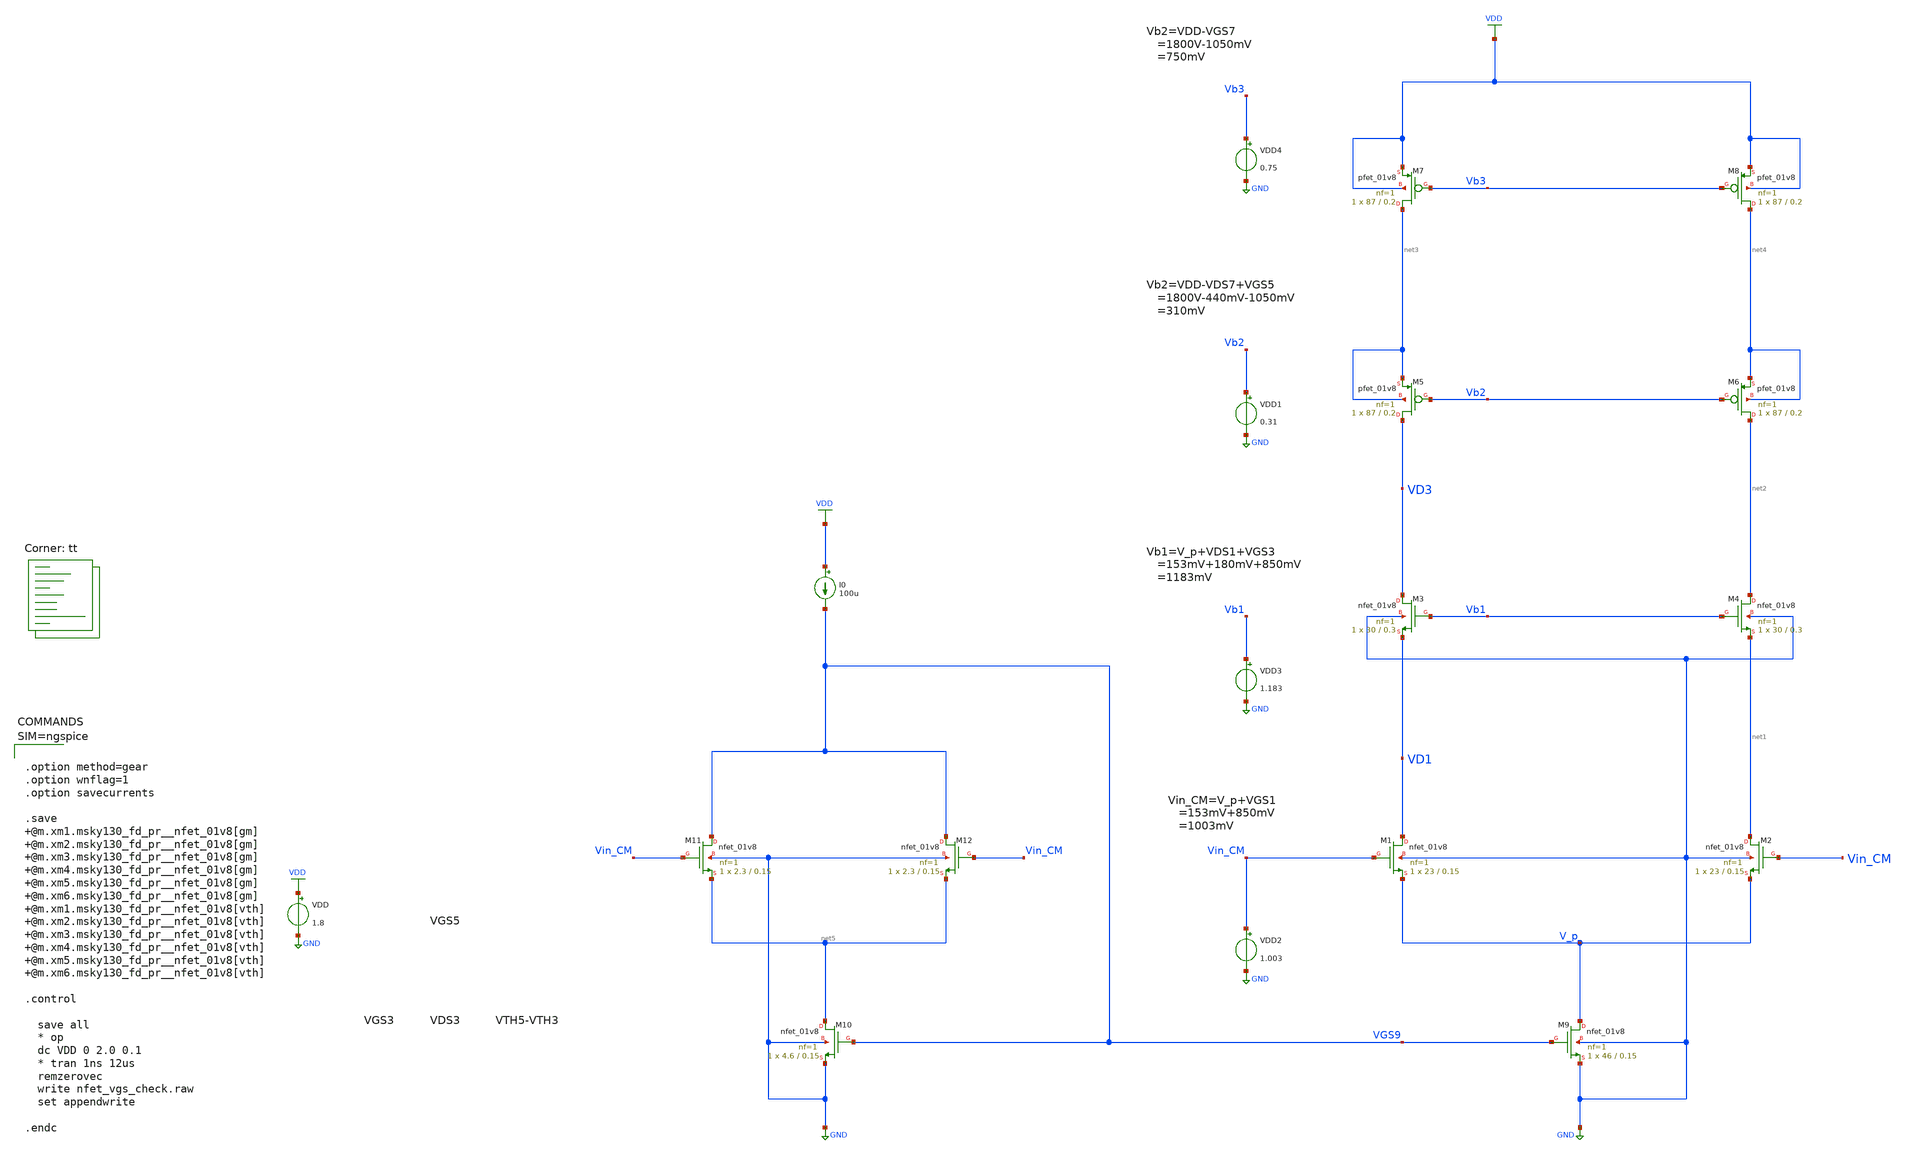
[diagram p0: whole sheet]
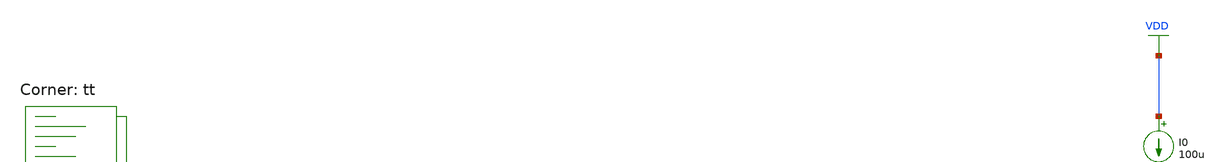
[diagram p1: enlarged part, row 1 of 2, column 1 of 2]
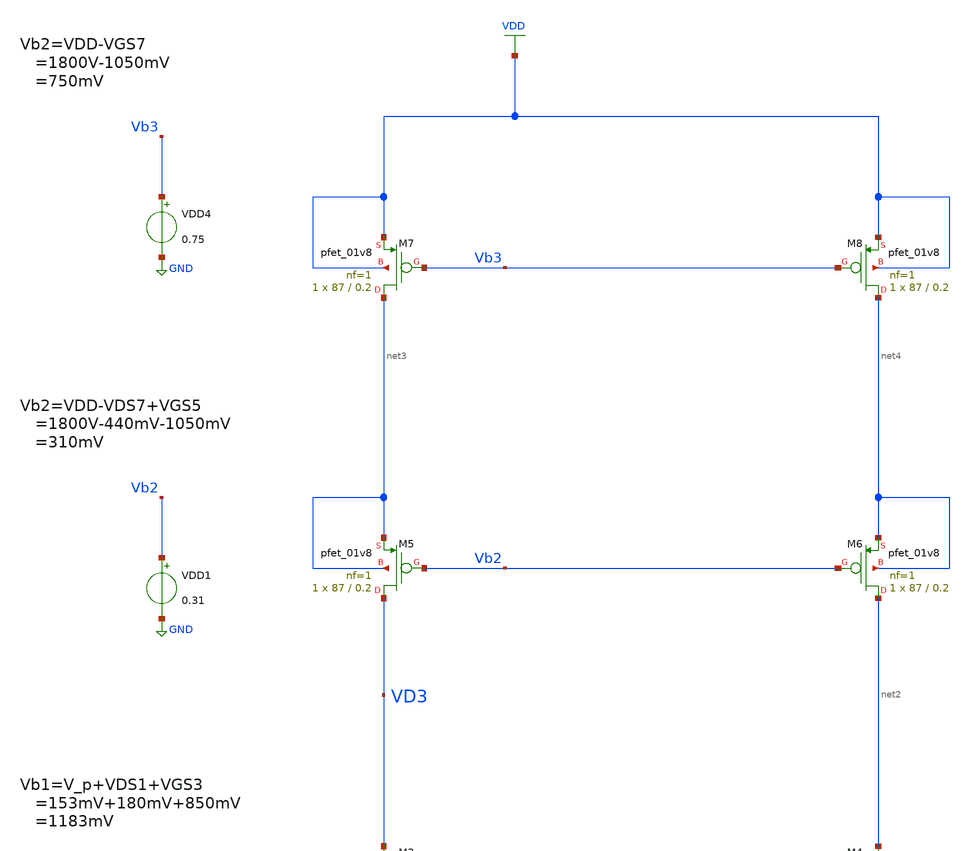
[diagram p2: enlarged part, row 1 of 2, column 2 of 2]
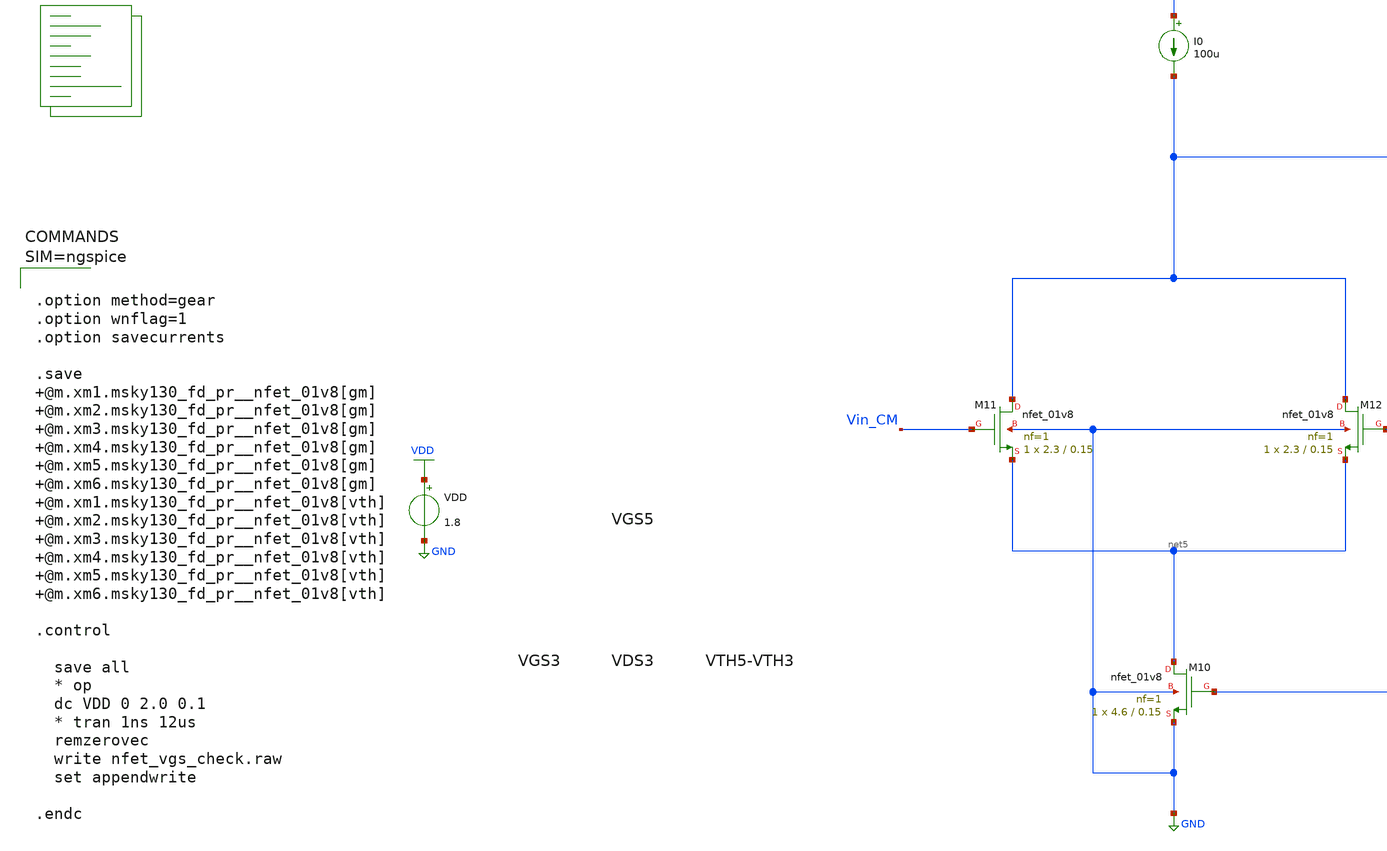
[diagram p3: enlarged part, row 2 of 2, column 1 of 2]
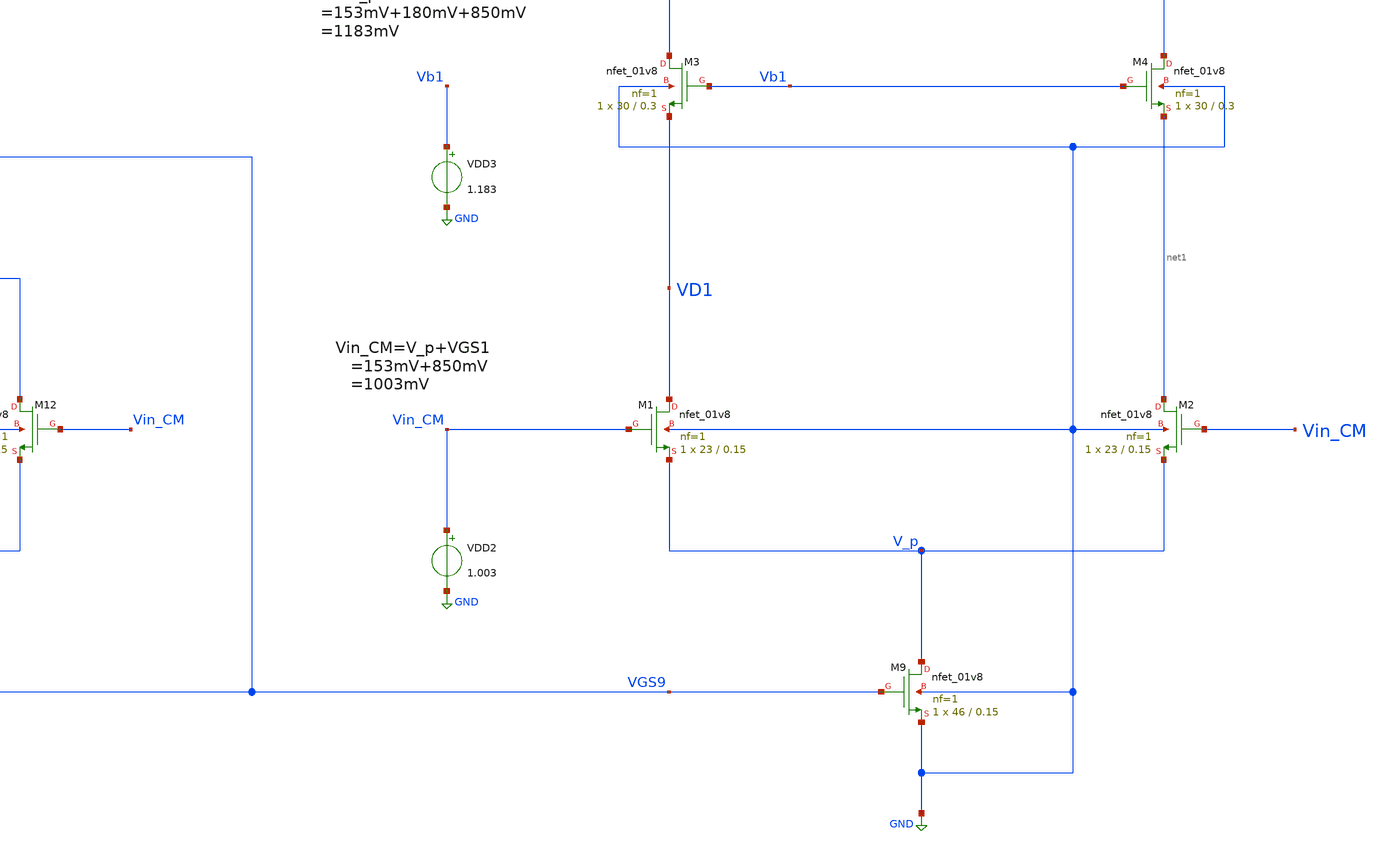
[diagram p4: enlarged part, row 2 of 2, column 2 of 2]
** sch_path: projects/opamp/xschem_ngspice/nfet_vgs_check.sch
**.subckt nfet_vgs_check
VDD VDD GND 1.8
XM1 VD1 Vin_CM V_p GND sky130_fd_pr__nfet_01v8 L=0.15 W=23 nf=1 ad='int((nf+1)/2) * W/nf * 0.29' as='int((nf+2)/2) * W/nf * 0.29'
+ pd='2*int((nf+1)/2) * (W/nf + 0.29)' ps='2*int((nf+2)/2) * (W/nf + 0.29)' nrd='0.29 / W' nrs='0.29 / W'
+ sa=0 sb=0 sd=0 mult=1 m=1
XM2 net1 Vin_CM V_p GND sky130_fd_pr__nfet_01v8 L=0.15 W=23 nf=1 ad='int((nf+1)/2) * W/nf * 0.29' as='int((nf+2)/2) * W/nf * 0.29'
+ pd='2*int((nf+1)/2) * (W/nf + 0.29)' ps='2*int((nf+2)/2) * (W/nf + 0.29)' nrd='0.29 / W' nrs='0.29 / W'
+ sa=0 sb=0 sd=0 mult=1 m=1
XM3 VD3 Vb1 VD1 GND sky130_fd_pr__nfet_01v8 L=0.3 W=30 nf=1 ad='int((nf+1)/2) * W/nf * 0.29' as='int((nf+2)/2) * W/nf * 0.29'
+ pd='2*int((nf+1)/2) * (W/nf + 0.29)' ps='2*int((nf+2)/2) * (W/nf + 0.29)' nrd='0.29 / W' nrs='0.29 / W'
+ sa=0 sb=0 sd=0 mult=1 m=1
XM4 net2 Vb1 net1 GND sky130_fd_pr__nfet_01v8 L=0.3 W=30 nf=1 ad='int((nf+1)/2) * W/nf * 0.29' as='int((nf+2)/2) * W/nf * 0.29'
+ pd='2*int((nf+1)/2) * (W/nf + 0.29)' ps='2*int((nf+2)/2) * (W/nf + 0.29)' nrd='0.29 / W' nrs='0.29 / W'
+ sa=0 sb=0 sd=0 mult=1 m=1
XM5 VD3 Vb2 net3 net3 sky130_fd_pr__pfet_01v8 L=0.2 W=87 nf=1 ad='int((nf+1)/2) * W/nf * 0.29' as='int((nf+2)/2) * W/nf * 0.29'
+ pd='2*int((nf+1)/2) * (W/nf + 0.29)' ps='2*int((nf+2)/2) * (W/nf + 0.29)' nrd='0.29 / W' nrs='0.29 / W'
+ sa=0 sb=0 sd=0 mult=1 m=1
XM6 net2 Vb2 net4 net4 sky130_fd_pr__pfet_01v8 L=0.2 W=87 nf=1 ad='int((nf+1)/2) * W/nf * 0.29' as='int((nf+2)/2) * W/nf * 0.29'
+ pd='2*int((nf+1)/2) * (W/nf + 0.29)' ps='2*int((nf+2)/2) * (W/nf + 0.29)' nrd='0.29 / W' nrs='0.29 / W'
+ sa=0 sb=0 sd=0 mult=1 m=1
XM7 net3 Vb3 VDD VDD sky130_fd_pr__pfet_01v8 L=0.2 W=87 nf=1 ad='int((nf+1)/2) * W/nf * 0.29' as='int((nf+2)/2) * W/nf * 0.29'
+ pd='2*int((nf+1)/2) * (W/nf + 0.29)' ps='2*int((nf+2)/2) * (W/nf + 0.29)' nrd='0.29 / W' nrs='0.29 / W'
+ sa=0 sb=0 sd=0 mult=1 m=1
XM8 net4 Vb3 VDD VDD sky130_fd_pr__pfet_01v8 L=0.2 W=87 nf=1 ad='int((nf+1)/2) * W/nf * 0.29' as='int((nf+2)/2) * W/nf * 0.29'
+ pd='2*int((nf+1)/2) * (W/nf + 0.29)' ps='2*int((nf+2)/2) * (W/nf + 0.29)' nrd='0.29 / W' nrs='0.29 / W'
+ sa=0 sb=0 sd=0 mult=1 m=1
XM9 V_p VGS9 GND GND sky130_fd_pr__nfet_01v8 L=0.15 W=46 nf=1 ad='int((nf+1)/2) * W/nf * 0.29' as='int((nf+2)/2) * W/nf * 0.29'
+ pd='2*int((nf+1)/2) * (W/nf + 0.29)' ps='2*int((nf+2)/2) * (W/nf + 0.29)' nrd='0.29 / W' nrs='0.29 / W'
+ sa=0 sb=0 sd=0 mult=1 m=1
VDD2 Vin_CM GND 1.003
VDD3 Vb1 GND 1.183
VDD1 Vb2 GND 0.31
VDD4 Vb3 GND 0.75
XM10 net5 VGS9 GND GND sky130_fd_pr__nfet_01v8 L=0.15 W=4.6 nf=1 ad='int((nf+1)/2) * W/nf * 0.29' as='int((nf+2)/2) * W/nf * 0.29'
+ pd='2*int((nf+1)/2) * (W/nf + 0.29)' ps='2*int((nf+2)/2) * (W/nf + 0.29)' nrd='0.29 / W' nrs='0.29 / W'
+ sa=0 sb=0 sd=0 mult=1 m=1
I0 VDD VGS9 100u
XM11 VGS9 Vin_CM net5 GND sky130_fd_pr__nfet_01v8 L=0.15 W=2.3 nf=1 ad='int((nf+1)/2) * W/nf * 0.29'
+ as='int((nf+2)/2) * W/nf * 0.29' pd='2*int((nf+1)/2) * (W/nf + 0.29)' ps='2*int((nf+2)/2) * (W/nf + 0.29)'
+ nrd='0.29 / W' nrs='0.29 / W' sa=0 sb=0 sd=0 mult=1 m=1
XM12 VGS9 Vin_CM net5 GND sky130_fd_pr__nfet_01v8 L=0.15 W=2.3 nf=1 ad='int((nf+1)/2) * W/nf * 0.29'
+ as='int((nf+2)/2) * W/nf * 0.29' pd='2*int((nf+1)/2) * (W/nf + 0.29)' ps='2*int((nf+2)/2) * (W/nf + 0.29)'
+ nrd='0.29 / W' nrs='0.29 / W' sa=0 sb=0 sd=0 mult=1 m=1
**** begin user architecture code



.option method=gear
.option wnflag=1
.option savecurrents

.save @m.xm1.msky130_fd_pr__nfet_01v8[gm] @m.xm2.msky130_fd_pr__nfet_01v8[gm] @m.xm3.msky130_fd_pr__nfet_01v8[gm] @m.xm4.msky130_fd_pr__nfet_01v8[gm] @m.xm5.msky130_fd_pr__nfet_01v8[gm] @m.xm6.msky130_fd_pr__nfet_01v8[gm] @m.xm1.msky130_fd_pr__nfet_01v8[vth] @m.xm2.msky130_fd_pr__nfet_01v8[vth] @m.xm3.msky130_fd_pr__nfet_01v8[vth] @m.xm4.msky130_fd_pr__nfet_01v8[vth] @m.xm5.msky130_fd_pr__nfet_01v8[vth] @m.xm6.msky130_fd_pr__nfet_01v8[vth]

.control

  save all
  * op
  dc VDD 0 2.0 0.1
  * tran 1ns 12us
  remzerovec
  write nfet_vgs_check.raw
  set appendwrite

.endc




.lib $::SKYWATER_MODELS/sky130.lib.spice tt
**** end user architecture code
**.ends
.GLOBAL GND
.GLOBAL VDD
.end
